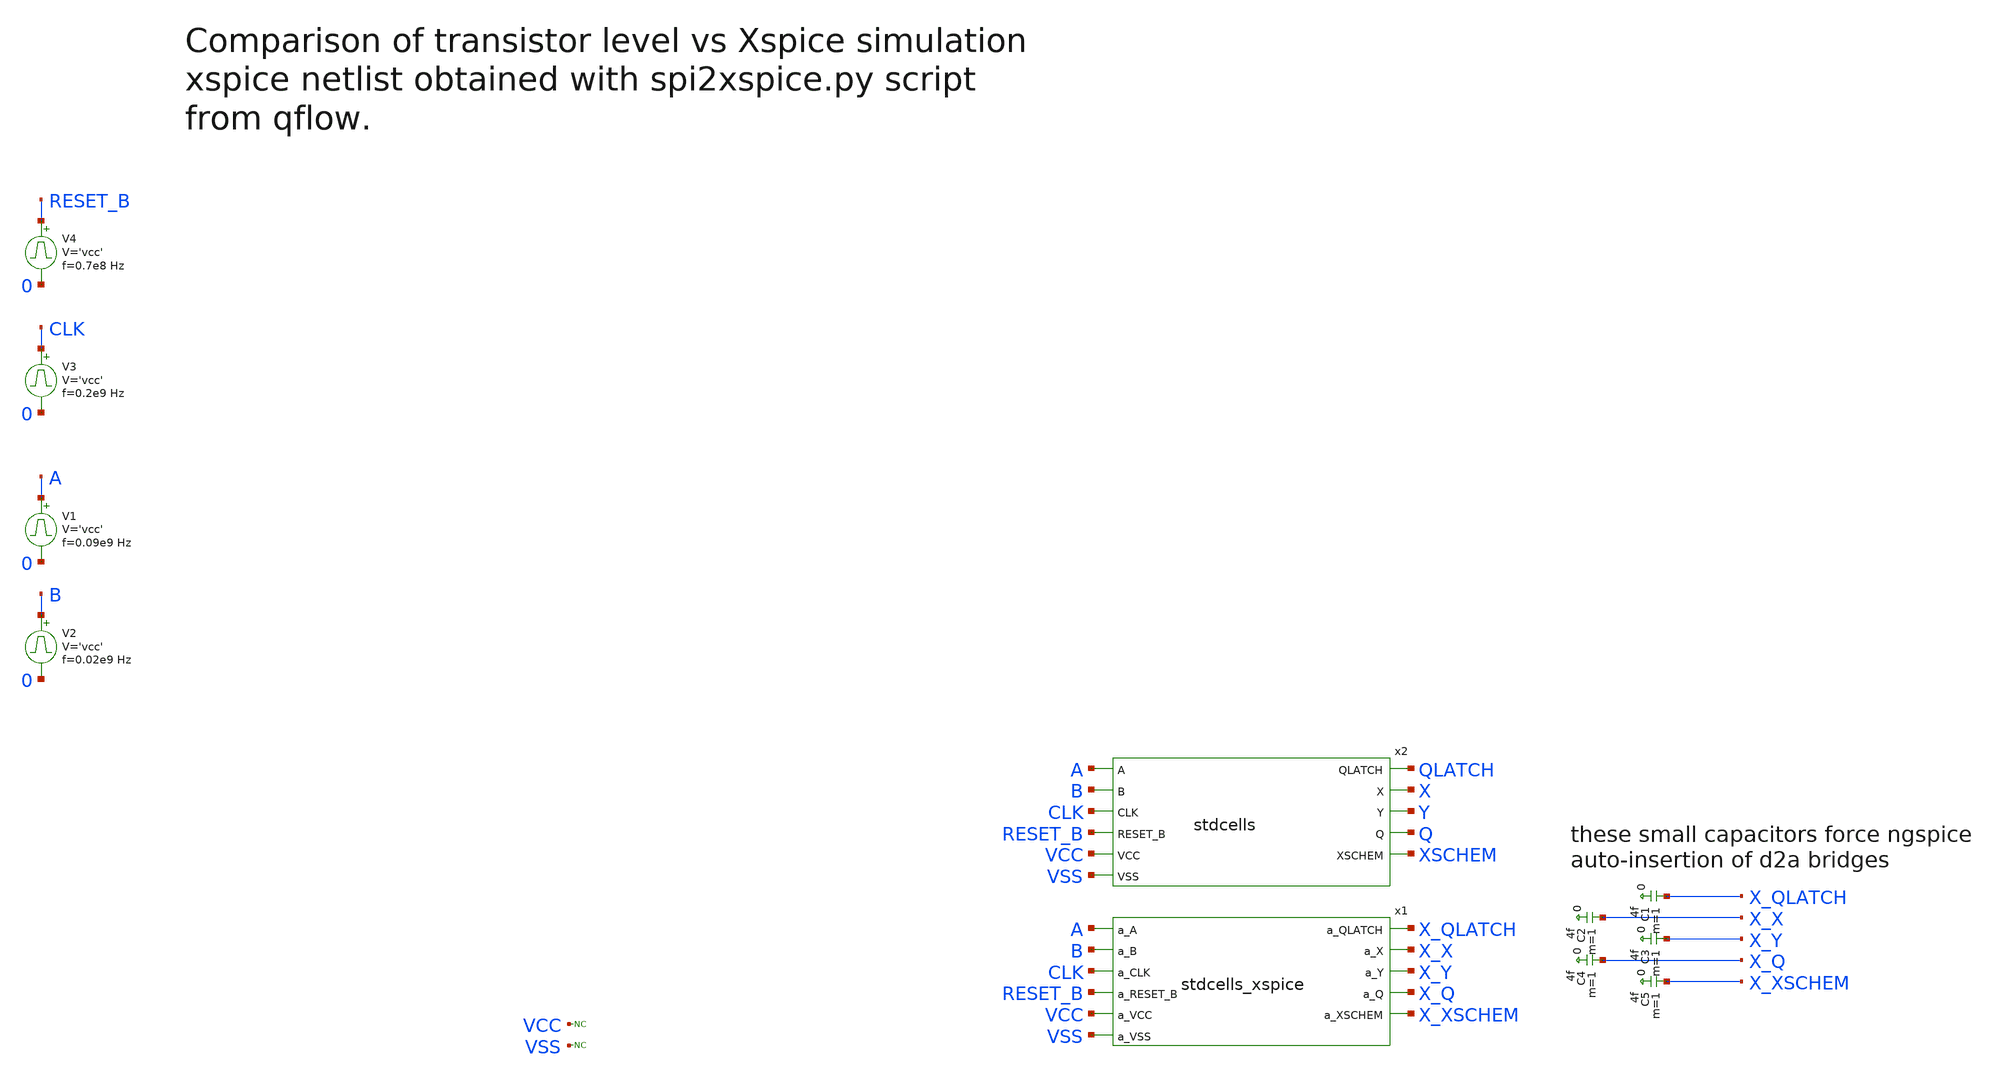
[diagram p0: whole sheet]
** sch_path: sky130A/xschem_libs/sky130_tests_ase/test_stdcells/schematic/test_stdcells.sch
* Copyright 2021 Stefan Frederik Schippers
* Licensed under the Apache License, Version 2.0 (the "License");
* you may not use this file except in compliance with the License.
* You may obtain a copy of the License at
* https://www.apache.org/licenses/LICENSE-2.0
* Unless required by applicable law or agreed to in writing, software
* distributed under the License is distributed on an "AS IS" BASIS,
* WITHOUT WARRANTIES OR CONDITIONS OF ANY KIND, either express or implied.
* See the License for the specific language governing permissions and
* limitations under the License.
**.subckt test_stdcells
V1 A 0 pulse 0 'vcc' '0.495/ 0.09e9 ' '0.01/0.09e9 ' '0.01/0.09e9 ' '0.49/0.09e9 ' '1/0.09e9 '
V2 B 0 pulse 0 'vcc' '0.495/ 0.02e9 ' '0.01/0.02e9 ' '0.01/0.02e9 ' '0.49/0.02e9 ' '1/0.02e9 '
V3 CLK 0 pulse 0 'vcc' '0.495/ 0.2e9 ' '0.01/0.2e9 ' '0.01/0.2e9 ' '0.49/0.2e9 ' '1/0.2e9 '
V4 RESET_B 0 pulse 0 'vcc' '0.495/ 0.7e8 ' '0.01/0.7e8 ' '0.01/0.7e8 ' '0.49/0.7e8 ' '1/0.7e8 '
x2 QLATCH A X B Y CLK Q RESET_B XSCHEM VCC VSS stdcells
x1 X_QLATCH A X_X B X_Y CLK X_Q RESET_B X_XSCHEM VCC VSS stdcells_xspice
* noconn VCC
* noconn VSS
C1 X_QLATCH 0 4f m=1
C2 X_X 0 4f m=1
C3 X_Y 0 4f m=1
C4 X_Q 0 4f m=1
C5 X_XSCHEM 0 4f m=1
**.ends

* expanding   symbol:  sky130_tests/stdcells.sym # of pins=11
** sym_path: sky130_tests/stdcells.sym
** sch_path: sky130_tests/stdcells.sch
.subckt stdcells QLATCH A X B Y CLK Q RESET_B XSCHEM VCC VSS
*.ipin RESET_B
*.ipin CLK
*.ipin B
*.ipin A
*.opin Y
*.opin X
*.opin QLATCH
*.opin Q
*.opin XSCHEM
*.ipin VCC
*.ipin VSS
x1 A B VSS VSS VCC VCC IX sky130_fd_sc_hd__nand2_1
C1 IX 0 3f m=1
x2 CLK A RESET_B VSS VSS VCC VCC IQ sky130_fd_sc_hd__dfrtp_1
C2 IQ 0 3f m=1
C3 IY 0 3f m=1
x3 A B VSS VSS VCC VCC IY sky130_fd_sc_hd__nor2b_1
x4 A CLK RESET_B VSS VSS VCC VCC IQLATCH net1 sky130_fd_sc_hd__dlrbn_1
C4 IQLATCH 0 3f m=1
x5 IY B VSS VSS VCC VCC net2 sky130_fd_sc_hd__nor2b_1
x6 net2 IQLATCH VSS VSS VCC VCC net4 sky130_fd_sc_hd__nand2_1
x7 net3 net4 IQ RESET_B VSS VSS VCC VCC IXSCHEM sky130_fd_sc_hd__a31o_2
* noconn #net1
* noconn IXSCHEM
x8 IY VSS VSS VCC VCC net3 sky130_fd_sc_hd__inv_2
x13 IY VSS VSS VCC VCC Y sky130_fd_sc_hd__buf_2
x9 IX VSS VSS VCC VCC X sky130_fd_sc_hd__buf_2
x14 IQ VSS VSS VCC VCC Q sky130_fd_sc_hd__buf_2
x15 IQLATCH VSS VSS VCC VCC QLATCH sky130_fd_sc_hd__buf_2
x11 IXSCHEM VSS VSS VCC VCC XSCHEM sky130_fd_sc_hd__buf_2
.ends


* expanding   symbol:  sky130_tests/stdcells_xspice.sym # of pins=11
** sym_path: sky130_tests/stdcells_xspice.sym
** sch_path: sky130_tests/stdcells_xspice.sch
.subckt stdcells_xspice a_QLATCH a_A a_X a_B a_Y a_CLK a_Q a_RESET_B a_XSCHEM a_VCC a_VSS
*.ipin a_RESET_B
*.ipin a_CLK
*.ipin a_B
*.ipin a_A
*.opin a_Y
*.opin a_X
*.opin a_QLATCH
*.opin a_Q
*.opin a_XSCHEM
*.ipin a_VCC
*.ipin a_VSS
**** begin user architecture code

A1 [A B] IX d_lut_sky130_fd_sc_hd__nand2_1
A2 A CLK NULL ~RESET_B IQ NULL ddflop
A3 [A B] IY d_lut_sky130_fd_sc_hd__nor2b_1
A4 A ~CLK NULL ~RESET_B IQLATCH NULL dlatch
A5 [IY B] net2 d_lut_sky130_fd_sc_hd__nor2b_1
A6 [net2 IQLATCH] net4 d_lut_sky130_fd_sc_hd__nand2_1
A7 [net3 net4 IQ RESET_B] IXSCHEM d_lut_sky130_fd_sc_hd__a31o_2
A8 [IY] net3 d_lut_sky130_fd_sc_hd__inv_2
A13 [IY] Y d_lut_sky130_fd_sc_hd__buf_2
A9 [IX] X d_lut_sky130_fd_sc_hd__buf_2
A14 [IQ] Q d_lut_sky130_fd_sc_hd__buf_2
A15 [IQLATCH] QLATCH d_lut_sky130_fd_sc_hd__buf_2
A11 [IXSCHEM] XSCHEM d_lut_sky130_fd_sc_hd__buf_2

AD2A1 [QLATCH] [a_QLATCH] toana_1v8
AA2D1 [a_A] [A] todig_1v8
AD2A2 [X] [a_X] toana_1v8
AA2D2 [a_B] [B] todig_1v8
AD2A3 [Y] [a_Y] toana_1v8
AA2D3 [a_CLK] [CLK] todig_1v8
AD2A4 [Q] [a_Q] toana_1v8
AA2D4 [a_RESET_B] [RESET_B] todig_1v8
AD2A5 [XSCHEM] [a_XSCHEM] toana_1v8
AA2D5 [a_VCC] [VCC] todig_1v8
AA2D6 [a_VSS] [VSS] todig_1v8


**** end user architecture code
.ends

.end
